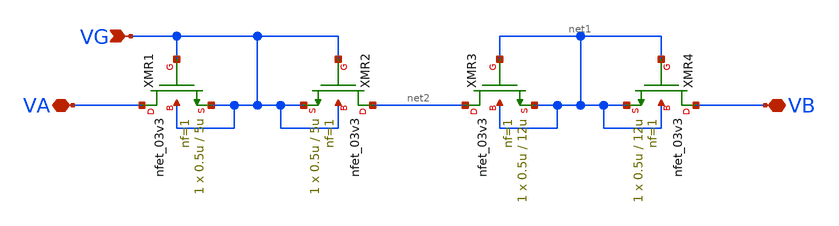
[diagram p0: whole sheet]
** sch_path: designs/libs/core_ina/ina_pseudores/ina_pseudores.sch
**.subckt ina_pseudores VG VA VB
*.ipin VG
*.iopin VA
*.iopin VB
XMR1 VA VG VG VG nfet_03v3 L=5u W=0.5u nf=1 ad='int((nf+1)/2) * W/nf * 0.18u' as='int((nf+2)/2) * W/nf * 0.18u'
+ pd='2*int((nf+1)/2) * (W/nf + 0.18u)' ps='2*int((nf+2)/2) * (W/nf + 0.18u)' nrd='0.18u / W' nrs='0.18u / W'
+ sa=0 sb=0 sd=0 m=1
XMR2 net2 VG VG VG nfet_03v3 L=5u W=0.5u nf=1 ad='int((nf+1)/2) * W/nf * 0.18u' as='int((nf+2)/2) * W/nf * 0.18u'
+ pd='2*int((nf+1)/2) * (W/nf + 0.18u)' ps='2*int((nf+2)/2) * (W/nf + 0.18u)' nrd='0.18u / W' nrs='0.18u / W'
+ sa=0 sb=0 sd=0 m=1
XMR3 net2 net1 net1 net1 nfet_03v3 L=12u W=0.5u nf=1 ad='int((nf+1)/2) * W/nf * 0.18u' as='int((nf+2)/2) * W/nf * 0.18u'
+ pd='2*int((nf+1)/2) * (W/nf + 0.18u)' ps='2*int((nf+2)/2) * (W/nf + 0.18u)' nrd='0.18u / W' nrs='0.18u / W'
+ sa=0 sb=0 sd=0 m=1
XMR4 VB net1 net1 net1 nfet_03v3 L=12u W=0.5u nf=1 ad='int((nf+1)/2) * W/nf * 0.18u' as='int((nf+2)/2) * W/nf * 0.18u'
+ pd='2*int((nf+1)/2) * (W/nf + 0.18u)' ps='2*int((nf+2)/2) * (W/nf + 0.18u)' nrd='0.18u / W' nrs='0.18u / W'
+ sa=0 sb=0 sd=0 m=1
**.ends
.end
